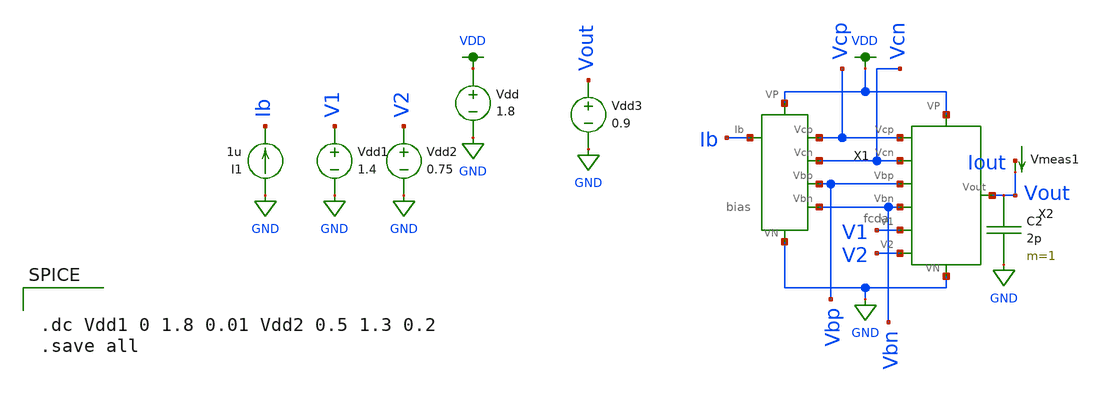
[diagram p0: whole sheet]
** sch_path: mp3/schematic/amp_tran.sch
**.subckt amp_tran
Vdd1 V1 GND 1.4
Vdd2 V2 GND 0.75
I1 GND Ib 1u
Vdd VDD GND 1.8
C2 Vout GND 2p m=1
X2 Vcp Vcn Vbp Vbn V1 V2 VDD GND Vout fcda
X1 VDD GND Ib Vcp Vcn Vbp Vbn bias
Vdd3 Vout GND 0.9
Vmeas1 Iout Vout 0
.save i(vmeas1)
**** begin user architecture code

.option wnflag=1
.lib ~/skywater/skywater-pdk/libraries/sky130_fd_pr_ngspice/latest/models/sky130.lib.spice tt



.dc Vdd1 0 1.8 0.01 Vdd2 0.5 1.3 0.2
.save all

**** end user architecture code
**.ends

* expanding   symbol:  /home/madvlsi/madvlsi/mp3/schematic/fcda.sym # of pins=9
** sym_path: mp3/schematic/fcda.sym
** sch_path: mp3/schematic/fcda.sch
.subckt fcda Vcp Vcn Vbp Vbn V1 V2 VP VN Vout
*.iopin VP
*.iopin VN
*.ipin Vbp
*.ipin V2
*.ipin V1
*.ipin Vbn
*.ipin Vcp
*.ipin Vcn
*.opin Vout
XM1 net2 Vbp VP VDD sky130_fd_pr__pfet_01v8 L=0.5 W=12 nf=1 ad='int((nf+1)/2) * W/nf * 0.29' as='int((nf+2)/2) * W/nf * 0.29'
+ pd='2*int((nf+1)/2) * (W/nf + 0.29)' ps='2*int((nf+2)/2) * (W/nf + 0.29)' nrd='0.29 / W' nrs='0.29 / W'
+ sa=0 sb=0 sd=0 mult=1 m=1
XM2 net2 V1 net1 GND sky130_fd_pr__nfet_01v8 L=0.5 W=12 nf=1 ad='int((nf+1)/2) * W/nf * 0.29' as='int((nf+2)/2) * W/nf * 0.29'
+ pd='2*int((nf+1)/2) * (W/nf + 0.29)' ps='2*int((nf+2)/2) * (W/nf + 0.29)' nrd='0.29 / W' nrs='0.29 / W'
+ sa=0 sb=0 sd=0 mult=1 m=1
XM3 net3 V2 net1 GND sky130_fd_pr__nfet_01v8 L=0.5 W=12 nf=1 ad='int((nf+1)/2) * W/nf * 0.29' as='int((nf+2)/2) * W/nf * 0.29'
+ pd='2*int((nf+1)/2) * (W/nf + 0.29)' ps='2*int((nf+2)/2) * (W/nf + 0.29)' nrd='0.29 / W' nrs='0.29 / W'
+ sa=0 sb=0 sd=0 mult=1 m=1
XM4 net1 Vbn VN GND sky130_fd_pr__nfet_01v8 L=0.5 W=12 nf=1 ad='int((nf+1)/2) * W/nf * 0.29' as='int((nf+2)/2) * W/nf * 0.29'
+ pd='2*int((nf+1)/2) * (W/nf + 0.29)' ps='2*int((nf+2)/2) * (W/nf + 0.29)' nrd='0.29 / W' nrs='0.29 / W'
+ sa=0 sb=0 sd=0 mult=1 m=1
XM5 net3 Vbp VP VDD sky130_fd_pr__pfet_01v8 L=0.5 W=12 nf=1 ad='int((nf+1)/2) * W/nf * 0.29' as='int((nf+2)/2) * W/nf * 0.29'
+ pd='2*int((nf+1)/2) * (W/nf + 0.29)' ps='2*int((nf+2)/2) * (W/nf + 0.29)' nrd='0.29 / W' nrs='0.29 / W'
+ sa=0 sb=0 sd=0 mult=1 m=1
XM6 Vout Vcp net3 VDD sky130_fd_pr__pfet_01v8 L=0.5 W=12 nf=1 ad='int((nf+1)/2) * W/nf * 0.29' as='int((nf+2)/2) * W/nf * 0.29'
+ pd='2*int((nf+1)/2) * (W/nf + 0.29)' ps='2*int((nf+2)/2) * (W/nf + 0.29)' nrd='0.29 / W' nrs='0.29 / W'
+ sa=0 sb=0 sd=0 mult=1 m=1
XM7 net4 Vcp net2 VDD sky130_fd_pr__pfet_01v8 L=0.5 W=12 nf=1 ad='int((nf+1)/2) * W/nf * 0.29' as='int((nf+2)/2) * W/nf * 0.29'
+ pd='2*int((nf+1)/2) * (W/nf + 0.29)' ps='2*int((nf+2)/2) * (W/nf + 0.29)' nrd='0.29 / W' nrs='0.29 / W'
+ sa=0 sb=0 sd=0 mult=1 m=1
XM8 net4 Vcn net5 GND sky130_fd_pr__nfet_01v8 L=0.5 W=12 nf=1 ad='int((nf+1)/2) * W/nf * 0.29' as='int((nf+2)/2) * W/nf * 0.29'
+ pd='2*int((nf+1)/2) * (W/nf + 0.29)' ps='2*int((nf+2)/2) * (W/nf + 0.29)' nrd='0.29 / W' nrs='0.29 / W'
+ sa=0 sb=0 sd=0 mult=1 m=1
XM9 net6 net4 VN GND sky130_fd_pr__nfet_01v8 L=0.5 W=12 nf=1 ad='int((nf+1)/2) * W/nf * 0.29' as='int((nf+2)/2) * W/nf * 0.29'
+ pd='2*int((nf+1)/2) * (W/nf + 0.29)' ps='2*int((nf+2)/2) * (W/nf + 0.29)' nrd='0.29 / W' nrs='0.29 / W'
+ sa=0 sb=0 sd=0 mult=1 m=1
XM10 Vout Vcn net6 GND sky130_fd_pr__nfet_01v8 L=0.5 W=12 nf=1 ad='int((nf+1)/2) * W/nf * 0.29' as='int((nf+2)/2) * W/nf * 0.29'
+ pd='2*int((nf+1)/2) * (W/nf + 0.29)' ps='2*int((nf+2)/2) * (W/nf + 0.29)' nrd='0.29 / W' nrs='0.29 / W'
+ sa=0 sb=0 sd=0 mult=1 m=1
XM11 VN net4 net5 GND sky130_fd_pr__nfet_01v8 L=0.5 W=12 nf=1 ad='int((nf+1)/2) * W/nf * 0.29' as='int((nf+2)/2) * W/nf * 0.29'
+ pd='2*int((nf+1)/2) * (W/nf + 0.29)' ps='2*int((nf+2)/2) * (W/nf + 0.29)' nrd='0.29 / W' nrs='0.29 / W'
+ sa=0 sb=0 sd=0 mult=1 m=1
.ends


* expanding   symbol:  /home/madvlsi/madvlsi/mp3/schematic/bias.sym # of pins=7
** sym_path: mp3/schematic/bias.sym
** sch_path: mp3/schematic/bias.sch
.subckt bias VP VN Ib Vcp Vcn Vbp Vbn
*.iopin VP
*.iopin VN
*.opin Vcp
*.opin Vcn
*.opin Vbp
*.iopin Ib
*.opin Vbn
XM1 net3 net1 VP VDD sky130_fd_pr__pfet_01v8 L=0.5 W=12 nf=1 ad='int((nf+1)/2) * W/nf * 0.29' as='int((nf+2)/2) * W/nf * 0.29'
+ pd='2*int((nf+1)/2) * (W/nf + 0.29)' ps='2*int((nf+2)/2) * (W/nf + 0.29)' nrd='0.29 / W' nrs='0.29 / W'
+ sa=0 sb=0 sd=0 mult=1 m=1
XM2 net1 net1 net3 VDD sky130_fd_pr__pfet_01v8 L=0.5 W=12 nf=1 ad='int((nf+1)/2) * W/nf * 0.29' as='int((nf+2)/2) * W/nf * 0.29'
+ pd='2*int((nf+1)/2) * (W/nf + 0.29)' ps='2*int((nf+2)/2) * (W/nf + 0.29)' nrd='0.29 / W' nrs='0.29 / W'
+ sa=0 sb=0 sd=0 mult=4 m=4
XM3 net3 Vcp Vcp VDD sky130_fd_pr__pfet_01v8 L=0.5 W=12 nf=1 ad='int((nf+1)/2) * W/nf * 0.29' as='int((nf+2)/2) * W/nf * 0.29'
+ pd='2*int((nf+1)/2) * (W/nf + 0.29)' ps='2*int((nf+2)/2) * (W/nf + 0.29)' nrd='0.29 / W' nrs='0.29 / W'
+ sa=0 sb=0 sd=0 mult=1 m=1
XM4 net1 Ib VN GND sky130_fd_pr__nfet_01v8 L=0.5 W=12 nf=1 ad='int((nf+1)/2) * W/nf * 0.29' as='int((nf+2)/2) * W/nf * 0.29'
+ pd='2*int((nf+1)/2) * (W/nf + 0.29)' ps='2*int((nf+2)/2) * (W/nf + 0.29)' nrd='0.29 / W' nrs='0.29 / W'
+ sa=0 sb=0 sd=0 mult=1/6 m=1/6
XM5 Vcp Ib VN GND sky130_fd_pr__nfet_01v8 L=0.5 W=12 nf=1 ad='int((nf+1)/2) * W/nf * 0.29' as='int((nf+2)/2) * W/nf * 0.29'
+ pd='2*int((nf+1)/2) * (W/nf + 0.29)' ps='2*int((nf+2)/2) * (W/nf + 0.29)' nrd='0.29 / W' nrs='0.29 / W'
+ sa=0 sb=0 sd=0 mult=1 m=1
XM6 Vbp Ib VN GND sky130_fd_pr__nfet_01v8 L=0.5 W=12 nf=1 ad='int((nf+1)/2) * W/nf * 0.29' as='int((nf+2)/2) * W/nf * 0.29'
+ pd='2*int((nf+1)/2) * (W/nf + 0.29)' ps='2*int((nf+2)/2) * (W/nf + 0.29)' nrd='0.29 / W' nrs='0.29 / W'
+ sa=0 sb=0 sd=0 mult=1 m=1
XM7 Vbn Vbp VP VDD sky130_fd_pr__pfet_01v8 L=0.5 W=12 nf=1 ad='int((nf+1)/2) * W/nf * 0.29' as='int((nf+2)/2) * W/nf * 0.29'
+ pd='2*int((nf+1)/2) * (W/nf + 0.29)' ps='2*int((nf+2)/2) * (W/nf + 0.29)' nrd='0.29 / W' nrs='0.29 / W'
+ sa=0 sb=0 sd=0 mult=1/6 m=1/6
XM8 Vcn Vbp VP VDD sky130_fd_pr__pfet_01v8 L=0.5 W=12 nf=1 ad='int((nf+1)/2) * W/nf * 0.29' as='int((nf+2)/2) * W/nf * 0.29'
+ pd='2*int((nf+1)/2) * (W/nf + 0.29)' ps='2*int((nf+2)/2) * (W/nf + 0.29)' nrd='0.29 / W' nrs='0.29 / W'
+ sa=0 sb=0 sd=0 mult=1 m=1
XM9 net2 Vcn Vcn GND sky130_fd_pr__nfet_01v8 L=0.5 W=12 nf=1 ad='int((nf+1)/2) * W/nf * 0.29' as='int((nf+2)/2) * W/nf * 0.29'
+ pd='2*int((nf+1)/2) * (W/nf + 0.29)' ps='2*int((nf+2)/2) * (W/nf + 0.29)' nrd='0.29 / W' nrs='0.29 / W'
+ sa=0 sb=0 sd=0 mult=1 m=1
XM10 net2 Vbn VN GND sky130_fd_pr__nfet_01v8 L=0.5 W=12 nf=1 ad='int((nf+1)/2) * W/nf * 0.29' as='int((nf+2)/2) * W/nf * 0.29'
+ pd='2*int((nf+1)/2) * (W/nf + 0.29)' ps='2*int((nf+2)/2) * (W/nf + 0.29)' nrd='0.29 / W' nrs='0.29 / W'
+ sa=0 sb=0 sd=0 mult=1 m=1
XM11 Vbn Vbn net2 GND sky130_fd_pr__nfet_01v8 L=0.5 W=12 nf=1 ad='int((nf+1)/2) * W/nf * 0.29' as='int((nf+2)/2) * W/nf * 0.29'
+ pd='2*int((nf+1)/2) * (W/nf + 0.29)' ps='2*int((nf+2)/2) * (W/nf + 0.29)' nrd='0.29 / W' nrs='0.29 / W'
+ sa=0 sb=0 sd=0 mult=4 m=4
XM12 VN Ib Ib GND sky130_fd_pr__nfet_01v8 L=0.5 W=12 nf=1 ad='int((nf+1)/2) * W/nf * 0.29' as='int((nf+2)/2) * W/nf * 0.29'
+ pd='2*int((nf+1)/2) * (W/nf + 0.29)' ps='2*int((nf+2)/2) * (W/nf + 0.29)' nrd='0.29 / W' nrs='0.29 / W'
+ sa=0 sb=0 sd=0 mult=1 m=1
XM13 Vbp Vbp VP VDD sky130_fd_pr__pfet_01v8 L=0.5 W=12 nf=1 ad='int((nf+1)/2) * W/nf * 0.29' as='int((nf+2)/2) * W/nf * 0.29'
+ pd='2*int((nf+1)/2) * (W/nf + 0.29)' ps='2*int((nf+2)/2) * (W/nf + 0.29)' nrd='0.29 / W' nrs='0.29 / W'
+ sa=0 sb=0 sd=0 mult=1 m=1
.ends

.GLOBAL GND
.GLOBAL VDD
.end
